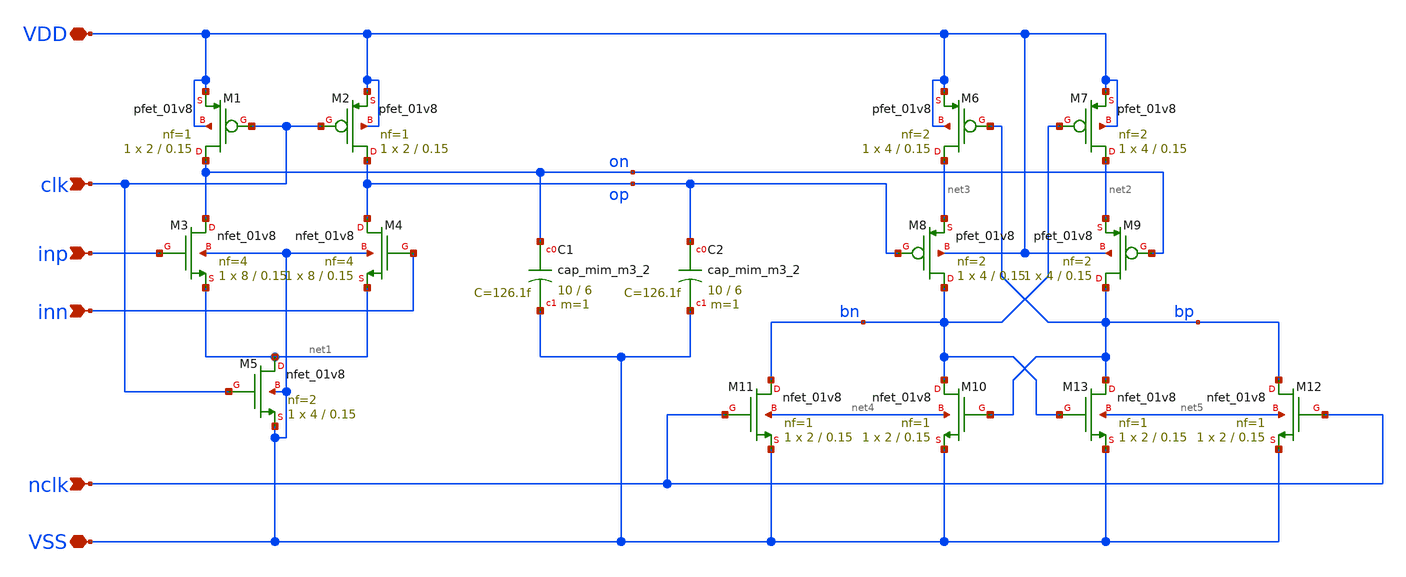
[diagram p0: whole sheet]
** sch_path: xschem/adc_comp/adc_comp.sch
**.subckt adc_comp VDD VSS inp inn clk nclk
*.iopin VDD
*.iopin VSS
*.ipin inp
*.ipin inn
*.ipin clk
*.ipin nclk
XM1 on clk VDD VDD sky130_fd_pr__pfet_01v8 L=0.15 W=2 nf=1 ad='int((nf+1)/2) * W/nf * 0.29' as='int((nf+2)/2) * W/nf * 0.29'
+ pd='2*int((nf+1)/2) * (W/nf + 0.29)' ps='2*int((nf+2)/2) * (W/nf + 0.29)' nrd='0.29 / W' nrs='0.29 / W'
+ sa=0 sb=0 sd=0 mult=1 m=1
XM2 op clk VDD VDD sky130_fd_pr__pfet_01v8 L=0.15 W=2 nf=1 ad='int((nf+1)/2) * W/nf * 0.29' as='int((nf+2)/2) * W/nf * 0.29'
+ pd='2*int((nf+1)/2) * (W/nf + 0.29)' ps='2*int((nf+2)/2) * (W/nf + 0.29)' nrd='0.29 / W' nrs='0.29 / W'
+ sa=0 sb=0 sd=0 mult=1 m=1
XM3 on inp net1 VSS sky130_fd_pr__nfet_01v8 L=0.15 W=8 nf=4 ad='int((nf+1)/2) * W/nf * 0.29' as='int((nf+2)/2) * W/nf * 0.29'
+ pd='2*int((nf+1)/2) * (W/nf + 0.29)' ps='2*int((nf+2)/2) * (W/nf + 0.29)' nrd='0.29 / W' nrs='0.29 / W'
+ sa=0 sb=0 sd=0 mult=1 m=1
XM4 op inn net1 VSS sky130_fd_pr__nfet_01v8 L=0.15 W=8 nf=4 ad='int((nf+1)/2) * W/nf * 0.29' as='int((nf+2)/2) * W/nf * 0.29'
+ pd='2*int((nf+1)/2) * (W/nf + 0.29)' ps='2*int((nf+2)/2) * (W/nf + 0.29)' nrd='0.29 / W' nrs='0.29 / W'
+ sa=0 sb=0 sd=0 mult=1 m=1
XM5 net1 clk VSS VSS sky130_fd_pr__nfet_01v8 L=0.15 W=4 nf=2 ad='int((nf+1)/2) * W/nf * 0.29' as='int((nf+2)/2) * W/nf * 0.29'
+ pd='2*int((nf+1)/2) * (W/nf + 0.29)' ps='2*int((nf+2)/2) * (W/nf + 0.29)' nrd='0.29 / W' nrs='0.29 / W'
+ sa=0 sb=0 sd=0 mult=1 m=1
XM6 net3 bp VDD VDD sky130_fd_pr__pfet_01v8 L=0.15 W=4 nf=2 ad='int((nf+1)/2) * W/nf * 0.29' as='int((nf+2)/2) * W/nf * 0.29'
+ pd='2*int((nf+1)/2) * (W/nf + 0.29)' ps='2*int((nf+2)/2) * (W/nf + 0.29)' nrd='0.29 / W' nrs='0.29 / W'
+ sa=0 sb=0 sd=0 mult=1 m=1
XM7 net2 bn VDD VDD sky130_fd_pr__pfet_01v8 L=0.15 W=4 nf=2 ad='int((nf+1)/2) * W/nf * 0.29' as='int((nf+2)/2) * W/nf * 0.29'
+ pd='2*int((nf+1)/2) * (W/nf + 0.29)' ps='2*int((nf+2)/2) * (W/nf + 0.29)' nrd='0.29 / W' nrs='0.29 / W'
+ sa=0 sb=0 sd=0 mult=1 m=1
XM8 bn op net3 VDD sky130_fd_pr__pfet_01v8 L=0.15 W=4 nf=2 ad='int((nf+1)/2) * W/nf * 0.29' as='int((nf+2)/2) * W/nf * 0.29'
+ pd='2*int((nf+1)/2) * (W/nf + 0.29)' ps='2*int((nf+2)/2) * (W/nf + 0.29)' nrd='0.29 / W' nrs='0.29 / W'
+ sa=0 sb=0 sd=0 mult=1 m=1
XM9 bp on net2 VDD sky130_fd_pr__pfet_01v8 L=0.15 W=4 nf=2 ad='int((nf+1)/2) * W/nf * 0.29' as='int((nf+2)/2) * W/nf * 0.29'
+ pd='2*int((nf+1)/2) * (W/nf + 0.29)' ps='2*int((nf+2)/2) * (W/nf + 0.29)' nrd='0.29 / W' nrs='0.29 / W'
+ sa=0 sb=0 sd=0 mult=1 m=1
XM10 bn bp VSS net4 sky130_fd_pr__nfet_01v8 L=0.15 W=2 nf=1 ad='int((nf+1)/2) * W/nf * 0.29' as='int((nf+2)/2) * W/nf * 0.29'
+ pd='2*int((nf+1)/2) * (W/nf + 0.29)' ps='2*int((nf+2)/2) * (W/nf + 0.29)' nrd='0.29 / W' nrs='0.29 / W'
+ sa=0 sb=0 sd=0 mult=1 m=1
XM11 bn nclk VSS net4 sky130_fd_pr__nfet_01v8 L=0.15 W=2 nf=1 ad='int((nf+1)/2) * W/nf * 0.29' as='int((nf+2)/2) * W/nf * 0.29'
+ pd='2*int((nf+1)/2) * (W/nf + 0.29)' ps='2*int((nf+2)/2) * (W/nf + 0.29)' nrd='0.29 / W' nrs='0.29 / W'
+ sa=0 sb=0 sd=0 mult=1 m=1
XM12 bp nclk VSS net5 sky130_fd_pr__nfet_01v8 L=0.15 W=2 nf=1 ad='int((nf+1)/2) * W/nf * 0.29' as='int((nf+2)/2) * W/nf * 0.29'
+ pd='2*int((nf+1)/2) * (W/nf + 0.29)' ps='2*int((nf+2)/2) * (W/nf + 0.29)' nrd='0.29 / W' nrs='0.29 / W'
+ sa=0 sb=0 sd=0 mult=1 m=1
XM13 bp bn VSS net5 sky130_fd_pr__nfet_01v8 L=0.15 W=2 nf=1 ad='int((nf+1)/2) * W/nf * 0.29' as='int((nf+2)/2) * W/nf * 0.29'
+ pd='2*int((nf+1)/2) * (W/nf + 0.29)' ps='2*int((nf+2)/2) * (W/nf + 0.29)' nrd='0.29 / W' nrs='0.29 / W'
+ sa=0 sb=0 sd=0 mult=1 m=1
XC1 on VSS sky130_fd_pr__cap_mim_m3_2 W=10 L=6 MF=1 m=1
XC2 op VSS sky130_fd_pr__cap_mim_m3_2 W=10 L=6 MF=1 m=1
**.ends
.end
